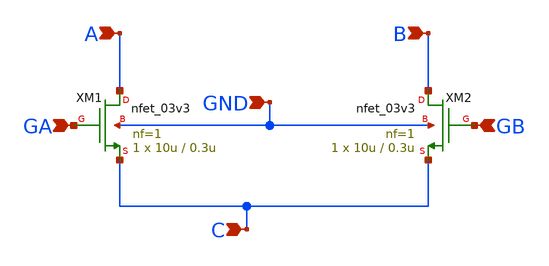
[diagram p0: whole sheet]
** sch_path: LDO/xschem/isource/diff.sch
**.subckt diff GA GB A B C GND
*.ipin GA
*.ipin GB
*.ipin A
*.ipin B
*.ipin C
*.ipin GND
XM1 A GA C GND nfet_03v3 L=0.3u W=10u nf=1 ad='int((nf+1)/2) * W/nf * 0.18u' as='int((nf+2)/2) * W/nf * 0.18u'
+ pd='2*int((nf+1)/2) * (W/nf + 0.18u)' ps='2*int((nf+2)/2) * (W/nf + 0.18u)' nrd='0.18u / W' nrs='0.18u / W'
+ sa=0 sb=0 sd=0 m=1
XM2 B GB C GND nfet_03v3 L=0.3u W=10u nf=1 ad='int((nf+1)/2) * W/nf * 0.18u' as='int((nf+2)/2) * W/nf * 0.18u'
+ pd='2*int((nf+1)/2) * (W/nf + 0.18u)' ps='2*int((nf+2)/2) * (W/nf + 0.18u)' nrd='0.18u / W' nrs='0.18u / W'
+ sa=0 sb=0 sd=0 m=1
**.ends
.end
